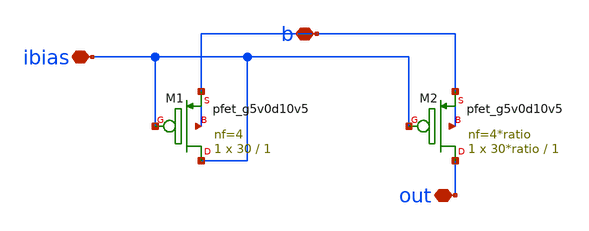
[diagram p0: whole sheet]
** sch_path: xschem/mosbius_lib/mosbius_psource.sch
**.subckt mosbius_psource ibias b out
*.iopin ibias
*.iopin b
*.iopin out
XM1 ibias ibias b b sky130_fd_pr__pfet_g5v0d10v5 L=1 W=30 nf=4 ad='int((nf+1)/2) * W/nf * 0.29' as='int((nf+2)/2) * W/nf * 0.29'
+ pd='2*int((nf+1)/2) * (W/nf + 0.29)' ps='2*int((nf+2)/2) * (W/nf + 0.29)' nrd='0.29 / W' nrs='0.29 / W'
+ sa=0 sb=0 sd=0 mult=1 m=1
XM2 out ibias b b sky130_fd_pr__pfet_g5v0d10v5 L=1 W=30*ratio nf=4*ratio ad='int((nf+1)/2) * W/nf * 0.29'
+ as='int((nf+2)/2) * W/nf * 0.29' pd='2*int((nf+1)/2) * (W/nf + 0.29)' ps='2*int((nf+2)/2) * (W/nf + 0.29)'
+ nrd='0.29 / W' nrs='0.29 / W' sa=0 sb=0 sd=0 mult=1 m=1
**.ends
.end
